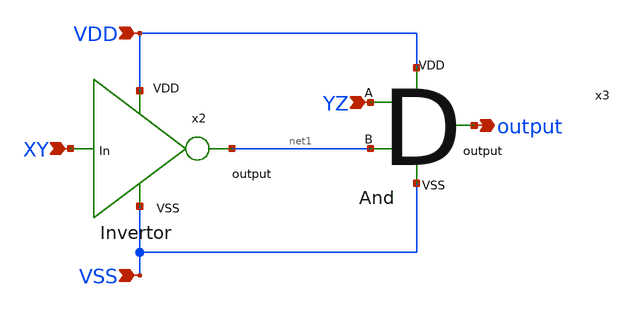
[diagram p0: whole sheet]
** sch_path: FINAL/XSCHEM/DECODER/yGates.sch
**.subckt yGates VDD VSS YZ XY output
*.ipin VDD
*.ipin VSS
*.ipin YZ
*.ipin XY
*.opin output
x2 VDD net1 XY VSS invertor
x3 YZ VDD net1 output VSS andGate
**.ends
.end
